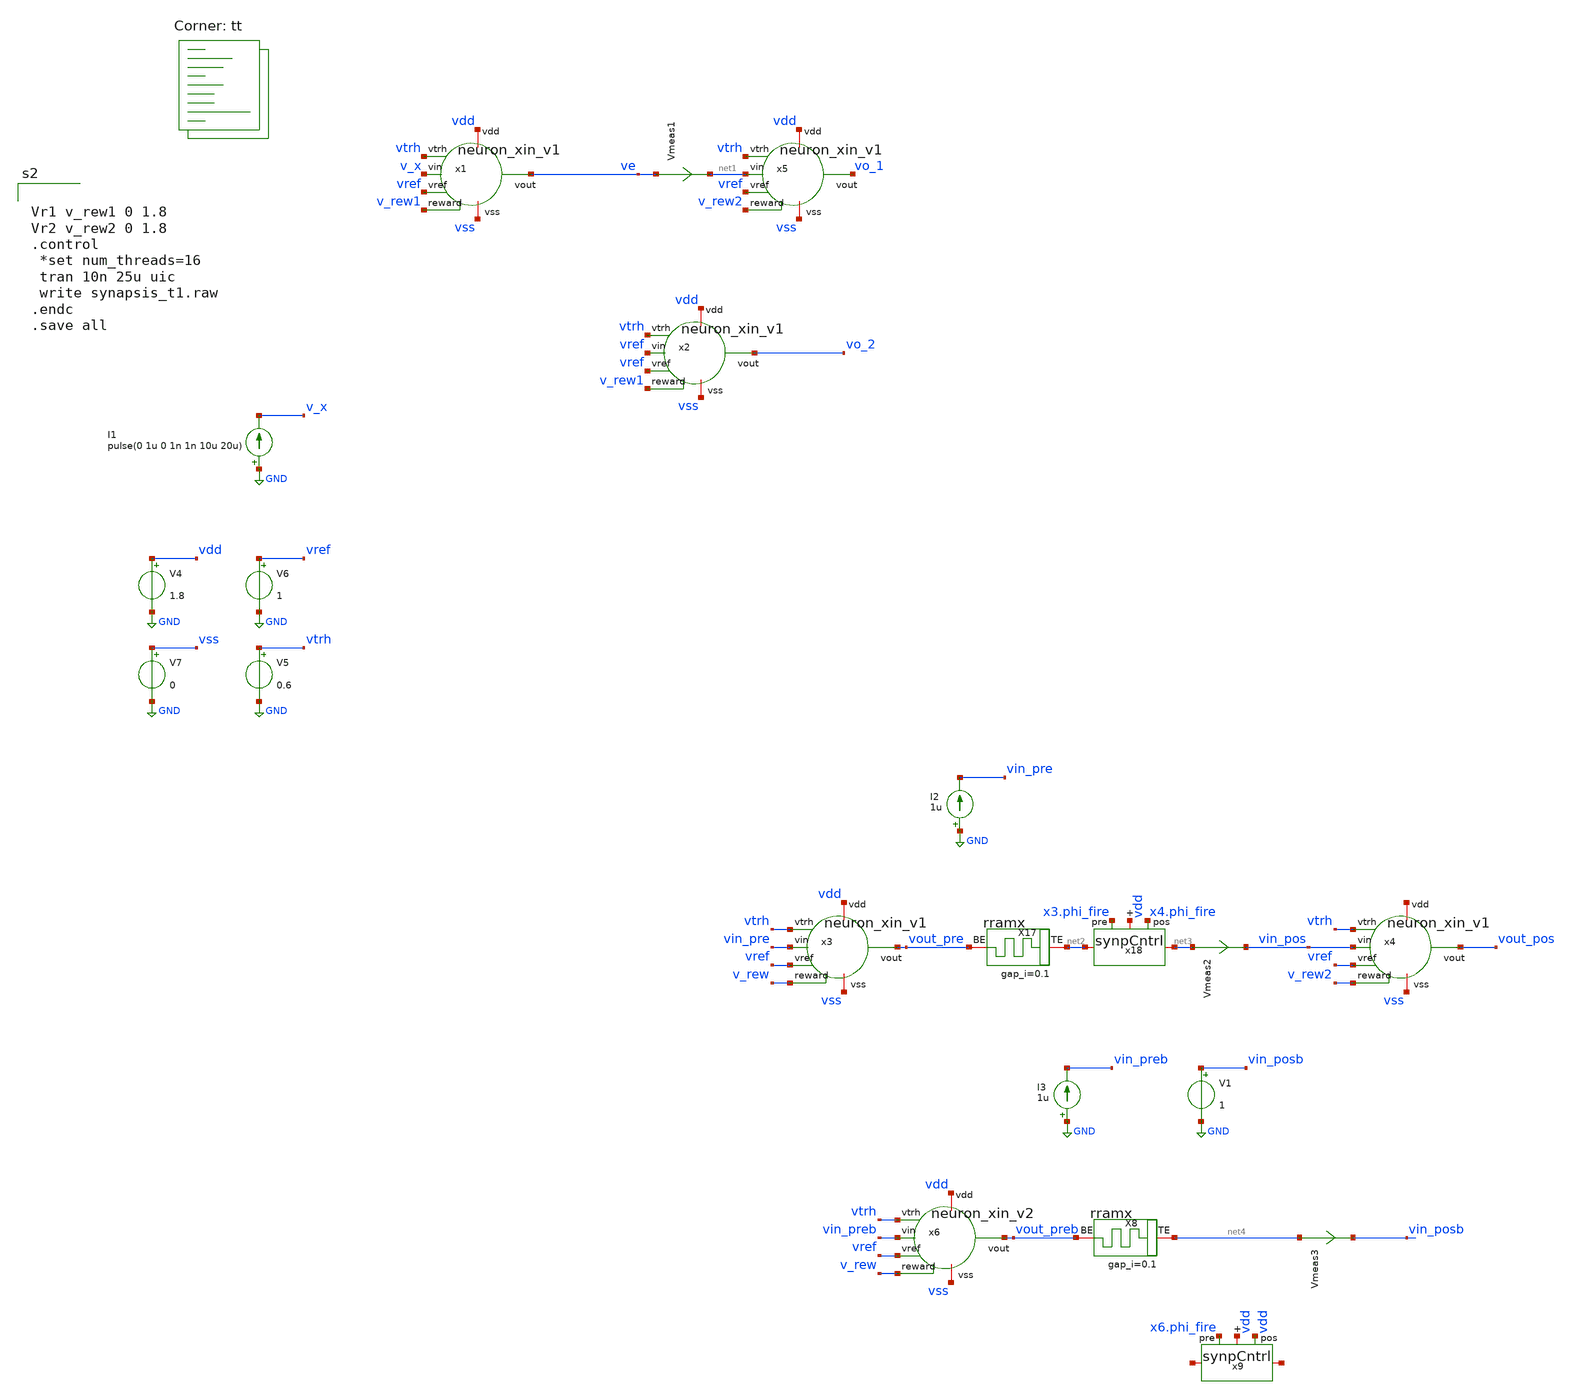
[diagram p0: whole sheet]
** sch_path: tests/synapsis_t1.sch
**.subckt synapsis_t1
V4 vdd GND 1.8
V5 vtrh GND 0.6
V6 vref GND 1
V7 vss GND 0
x1 vdd vss ve v_x vtrh vref v_rew1 neuron_xin_v1
x5 vdd vss vo_1 net1 vtrh vref v_rew2 neuron_xin_v1
x2 vdd vss vo_2 vref vtrh vref v_rew1 neuron_xin_v1
Vmeas1 ve net1 0
.save i(vmeas1)
I1 GND v_x pulse(0 1u 0 1n 1n 10u 20u)
Vmeas2 net3 vin_pos 0
.save i(vmeas2)
x3 vdd vss vout_pre vin_pre vtrh vref v_rew neuron_xin_v1
x4 net5 vss vout_pos vin_pos vtrh vref v_rew2 neuron_xin_v1
I2 GND vin_pre 1u
X17 net2 vout_pre rram_cell gap_i=0.1
x18 vdd x3.phi_fire x4.phi_fire net2 net3 synpCntrl
Vmeas3 net4 vin_posb 0
.save i(vmeas3)
I3 GND vin_preb 1u
X8 net4 vout_preb rram_cell gap_i=0.1
x9 vdd x6.phi_fire vdd net6 net7 synpCntrl
V1 vin_posb GND 1
x6 vdd vss vout_preb vin_preb vtrh vref v_rew neuron_xin_v2
**** begin user architecture code


Vr1 v_rew1 0 1.8
Vr2 v_rew2 0 1.8
.control
 *set num_threads=16
 tran 10n 25u uic
 write synapsis_t1.raw
.endc
.save all


.lib $::SKYWATER_MODELS/sky130.lib.spice tt

.subckt rram_cell BE TE gap_i=0.1
N1 BE TE rram_model
.model rram_model rram gap_initial={gap_i}
.ends rram_cell

.control
pre_osdi /foss/designs/spike_130/designs/prubs/rram.osdi
.endc

**** end user architecture code
**.ends
.GLOBAL GND
.end
